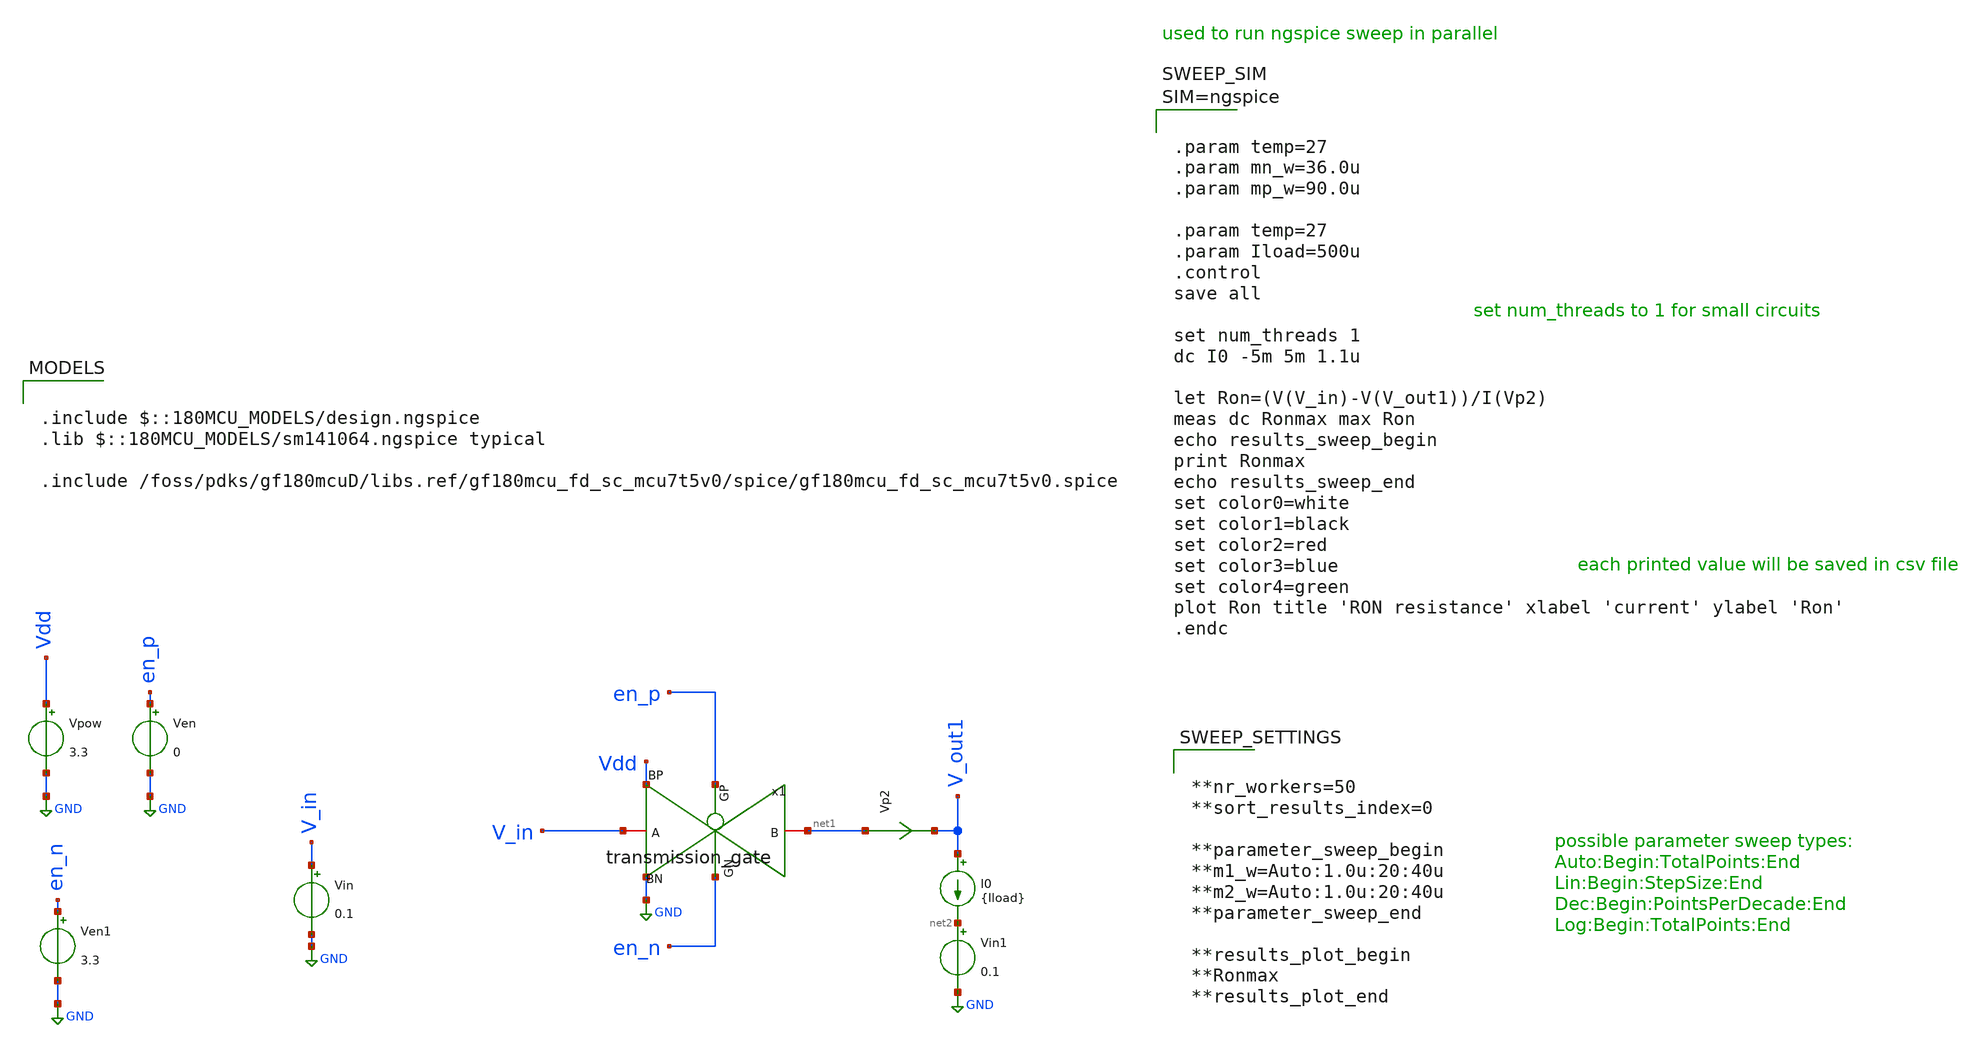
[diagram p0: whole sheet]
** sch_path: designs/switch_matrix_gf180mcu_9t5v0-main/tgate_PK/old/tgate_lv_isweep_tb.sch
**.subckt tgate_lv_isweep_tb
Vpow Vdd GND 3.3
Vin V_in GND 0.1
Ven en_p GND 0
Ven1 en_n GND 3.3
I0 V_out1 net2 {Iload}
Vp2 net1 V_out1 0
.save i(vp2)
Vin1 net2 GND 0.1
x1 net1 en_n en_p V_in Vdd GND transmission_gate
**** begin user architecture code



.param temp=27
.param mn_w=36.0u
.param mp_w=90.0u

.param temp=27
.param Iload=500u
.control
save all

set num_threads 1
dc I0 -5m 5m 1.1u

let Ron=(V(V_in)-V(V_out1))/I(Vp2)
meas dc Ronmax max Ron
echo results_sweep_begin
print Ronmax
echo results_sweep_end
set color0=white
set color1=black
set color2=red
set color3=blue
set color4=green
plot Ron title 'RON resistance' xlabel 'current' ylabel 'Ron'
.endc





**nr_workers=50
**sort_results_index=0

**parameter_sweep_begin
**m1_w=Auto:1.0u:20:40u
**m2_w=Auto:1.0u:20:40u
**parameter_sweep_end

**results_plot_begin
**Ronmax
**results_plot_end



.include $::180MCU_MODELS/design.ngspice
.lib $::180MCU_MODELS/sm141064.ngspice typical

.include /foss/pdks/gf180mcuD/libs.ref/gf180mcu_fd_sc_mcu7t5v0/spice/gf180mcu_fd_sc_mcu7t5v0.spice

**** end user architecture code
**.ends

* expanding   symbol:  transmission_gate.sym # of pins=6
** sym_path: designs/switch_matrix_gf180mcu_9t5v0-main/tgate_PK/transmission_gate.sym
** sch_path: designs/switch_matrix_gf180mcu_9t5v0-main/tgate_PK/transmission_gate.sch
.subckt transmission_gate B GN GP A BP BN
*.iopin B
*.iopin GN
*.iopin A
*.iopin GP
*.iopin BN
*.iopin BP
XM1 A GN B BN nfet_03v3 L=0.28u W=mn_w nf=6 ad='int((nf+1)/2) * W/nf * 0.18u' as='int((nf+2)/2) * W/nf * 0.18u'
+ pd='2*int((nf+1)/2) * (W/nf + 0.18u)' ps='2*int((nf+2)/2) * (W/nf + 0.18u)' nrd='0.18u / W' nrs='0.18u / W'
+ sa=0 sb=0 sd=0 m=1
XM2 A GP B BP pfet_03v3 L=0.28u W=mp_w nf=6 ad='int((nf+1)/2) * W/nf * 0.18u' as='int((nf+2)/2) * W/nf * 0.18u'
+ pd='2*int((nf+1)/2) * (W/nf + 0.18u)' ps='2*int((nf+2)/2) * (W/nf + 0.18u)' nrd='0.18u / W' nrs='0.18u / W'
+ sa=0 sb=0 sd=0 m=1
.ends

.GLOBAL GND
.end
